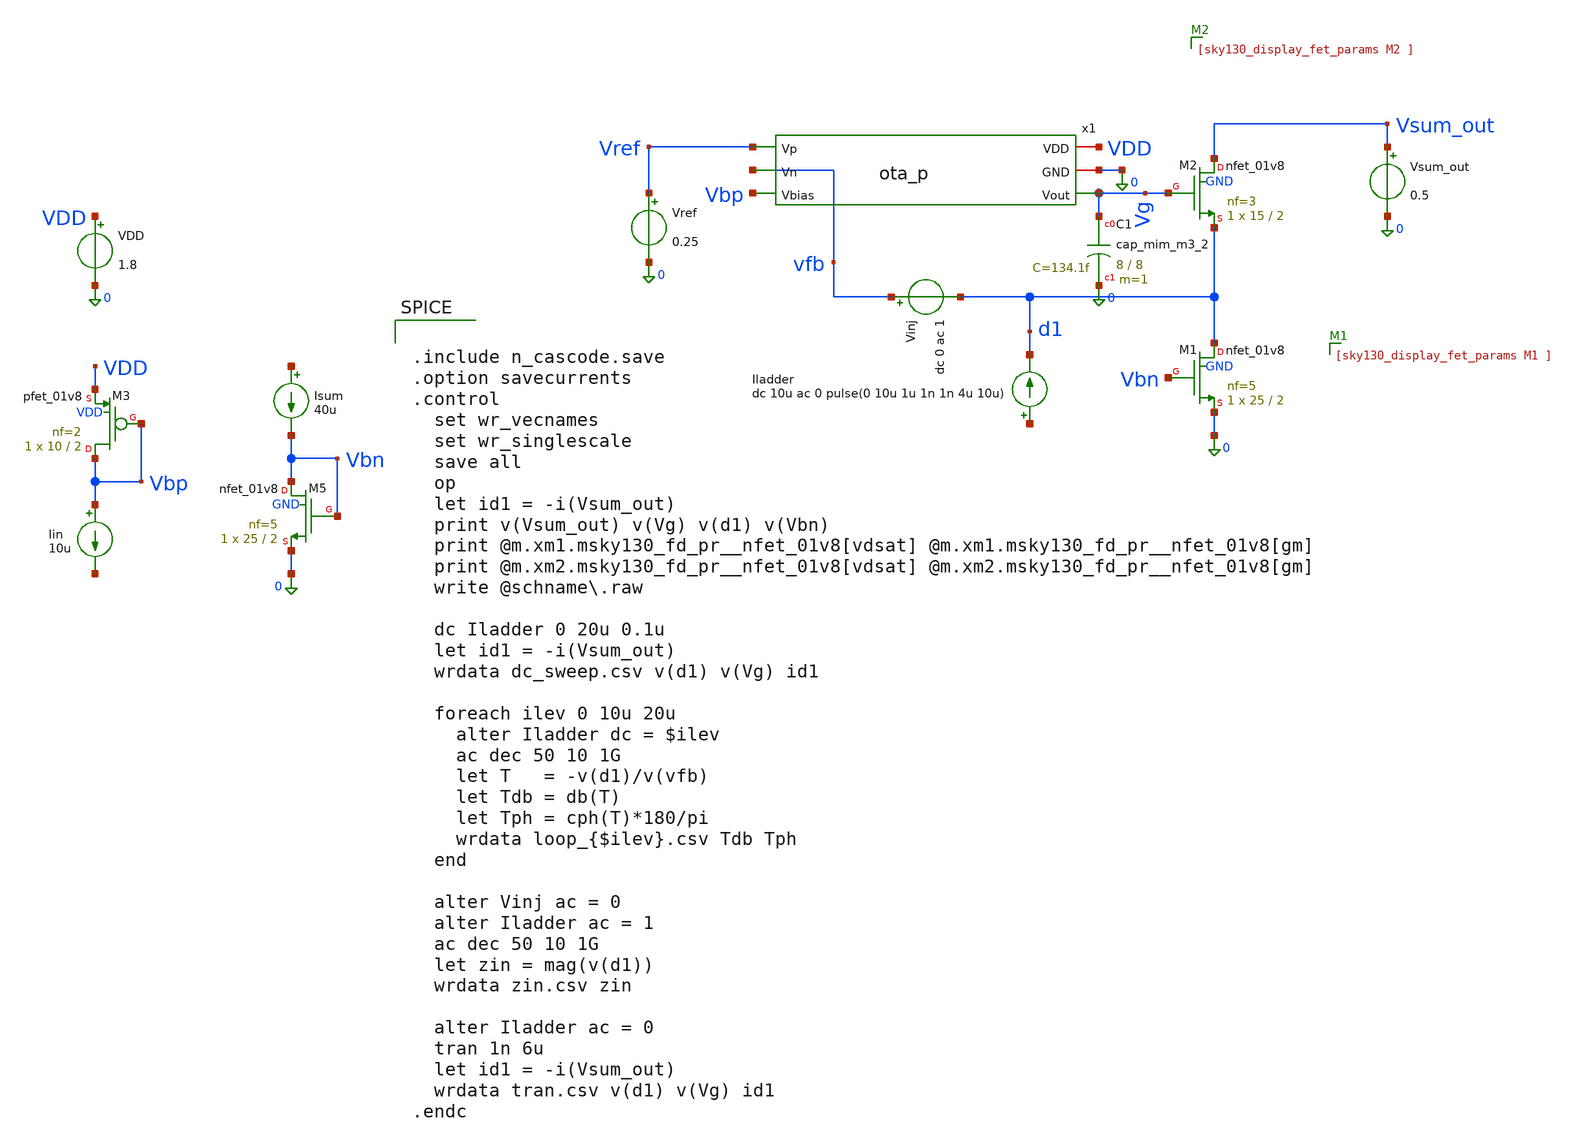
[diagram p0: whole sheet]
** sch_path: sch/cascode/n_cascode.sch
**.subckt n_cascode
XM1 d1 Vbn 0 GND sky130_fd_pr__nfet_01v8 L=2 W=25 nf=5 ad='int((5 + 1)/2) * 25 / 5 * 0.29' as='int((5 + 2)/2) * 25 / 5 * 0.29'
+ pd='2*int((5 + 1)/2) * (25 / 5 + 0.29)' ps='2*int((5 + 2)/2) * (25 / 5 + 0.29)' nrd='0.29 / 25 ' nrs='0.29 / 25 '
+ sa=0 sb=0 sd=0 mult=1 m=1
XM2 Vsum_out Vg d1 GND sky130_fd_pr__nfet_01v8 L=2 W=15 nf=3 ad='int((3 + 1)/2) * 15 / 3 * 0.29' as='int((3 + 2)/2) * 15 / 3 * 0.29'
+ pd='2*int((3 + 1)/2) * (15 / 3 + 0.29)' ps='2*int((3 + 2)/2) * (15 / 3 + 0.29)' nrd='0.29 / 15 ' nrs='0.29 / 15 '
+ sa=0 sb=0 sd=0 mult=1 m=1
x1 VDD 0 Vbp Vref vfb Vg ota_p
Vref Vref 0 0.25
.save i(vref)
VDD VDD 0 1.8
.save i(vdd)
Iin Vbp net1 10u
XM3 Vbp Vbp VDD VDD sky130_fd_pr__pfet_01v8 L=2 W=10 nf=2 ad='int((2 + 1)/2) * 10 / 2 * 0.29' as='int((2 + 2)/2) * 10 / 2 * 0.29'
+ pd='2*int((2 + 1)/2) * (10 / 2 + 0.29)' ps='2*int((2 + 2)/2) * (10 / 2 + 0.29)' nrd='0.29 / 10 ' nrs='0.29 / 10 '
+ sa=0 sb=0 sd=0 mult=1 m=1
Iladder net2 d1 dc 10u ac 0 pulse(0 10u 1u 1n 1n 4u 10u)
Isum net3 Vbn 40u
Vsum_out Vsum_out 0 0.5
.save i(vsum_out)
Vinj vfb d1 dc 0 ac 1
.save i(vinj)
XC1 Vg 0 sky130_fd_pr__cap_mim_m3_2 W=8 L=8 MF=1 m=1
XM5 Vbn Vbn 0 GND sky130_fd_pr__nfet_01v8 L=2 W=25 nf=5 ad='int((5 + 1)/2) * 25 / 5 * 0.29' as='int((5 + 2)/2) * 25 / 5 * 0.29'
+ pd='2*int((5 + 1)/2) * (25 / 5 + 0.29)' ps='2*int((5 + 2)/2) * (25 / 5 + 0.29)' nrd='0.29 / 25 ' nrs='0.29 / 25 '
+ sa=0 sb=0 sd=0 mult=1 m=1
**** begin user architecture code

** opencircuitdesign pdks install
.lib $::SKYWATER_MODELS/sky130.lib.spice tt
.include $::SKYWATER_STDCELLS/sky130_fd_sc_hd.spice



.include n_cascode.save
.option savecurrents
.control
  set wr_vecnames
  set wr_singlescale
  save all
  op
  let id1 = -i(Vsum_out)
  print v(Vsum_out) v(Vg) v(d1) v(Vbn)
  print @m.xm1.msky130_fd_pr__nfet_01v8[vdsat] @m.xm1.msky130_fd_pr__nfet_01v8[gm]
  print @m.xm2.msky130_fd_pr__nfet_01v8[vdsat] @m.xm2.msky130_fd_pr__nfet_01v8[gm]
  write @schname\.raw

  dc Iladder 0 20u 0.1u
  let id1 = -i(Vsum_out)
  wrdata dc_sweep.csv v(d1) v(Vg) id1

  foreach ilev 0 10u 20u
    alter Iladder dc = $ilev
    ac dec 50 10 1G
    let T   = -v(d1)/v(vfb)
    let Tdb = db(T)
    let Tph = cph(T)*180/pi
    wrdata loop_{$ilev}.csv Tdb Tph
  end

  alter Vinj ac = 0
  alter Iladder ac = 1
  ac dec 50 10 1G
  let zin = mag(v(d1))
  wrdata zin.csv zin

  alter Iladder ac = 0
  tran 1n 6u
  let id1 = -i(Vsum_out)
  wrdata tran.csv v(d1) v(Vg) id1
.endc


**** end user architecture code
**.ends

* expanding   symbol:  /foss/designs/sar_adc/sch/cascode/ota_p.sym # of pins=6
** sym_path: sch/cascode/ota_p.sym
** sch_path: sch/cascode/ota_p.sch
.subckt ota_p VDD GND Vbias Vp Vn Vout
*.ipin Vbias
*.opin Vout
*.iopin VDD
*.iopin GND
*.ipin Vp
*.ipin Vn
XM1 net1 Vp Vx VDD sky130_fd_pr__pfet_01v8 L=2 W=25 nf=5 ad='int((5 + 1)/2) * 25 / 5 * 0.29' as='int((5 + 2)/2) * 25 / 5 * 0.29'
+ pd='2*int((5 + 1)/2) * (25 / 5 + 0.29)' ps='2*int((5 + 2)/2) * (25 / 5 + 0.29)' nrd='0.29 / 25 ' nrs='0.29 / 25 '
+ sa=0 sb=0 sd=0 mult=1 m=1
XM2 Vout Vn Vx VDD sky130_fd_pr__pfet_01v8 L=2 W=25 nf=5 ad='int((5 + 1)/2) * 25 / 5 * 0.29' as='int((5 + 2)/2) * 25 / 5 * 0.29'
+ pd='2*int((5 + 1)/2) * (25 / 5 + 0.29)' ps='2*int((5 + 2)/2) * (25 / 5 + 0.29)' nrd='0.29 / 25 ' nrs='0.29 / 25 '
+ sa=0 sb=0 sd=0 mult=1 m=1
XM3 net1 net1 GND GND sky130_fd_pr__nfet_01v8 L=2 W=1.5 nf=1 ad='int((1 + 1)/2) * 1.5 / 1 * 0.29' as='int((1 + 2)/2) * 1.5 / 1 * 0.29'
+ pd='2*int((1 + 1)/2) * (1.5 / 1 + 0.29)' ps='2*int((1 + 2)/2) * (1.5 / 1 + 0.29)' nrd='0.29 / 1.5 ' nrs='0.29 / 1.5 '
+ sa=0 sb=0 sd=0 mult=1 m=1
XM4 Vout net1 GND GND sky130_fd_pr__nfet_01v8 L=2 W=1.5 nf=1 ad='int((1 + 1)/2) * 1.5 / 1 * 0.29' as='int((1 + 2)/2) * 1.5 / 1 * 0.29'
+ pd='2*int((1 + 1)/2) * (1.5 / 1 + 0.29)' ps='2*int((1 + 2)/2) * (1.5 / 1 + 0.29)' nrd='0.29 / 1.5 ' nrs='0.29 / 1.5 '
+ sa=0 sb=0 sd=0 mult=1 m=1
XM5 Vx Vbias VDD VDD sky130_fd_pr__pfet_01v8 L=2 W=10 nf=2 ad='int((2 + 1)/2) * 10 / 2 * 0.29' as='int((2 + 2)/2) * 10 / 2 * 0.29'
+ pd='2*int((2 + 1)/2) * (10 / 2 + 0.29)' ps='2*int((2 + 2)/2) * (10 / 2 + 0.29)' nrd='0.29 / 10 ' nrs='0.29 / 10 '
+ sa=0 sb=0 sd=0 mult=1 m=1
.ends

.end
